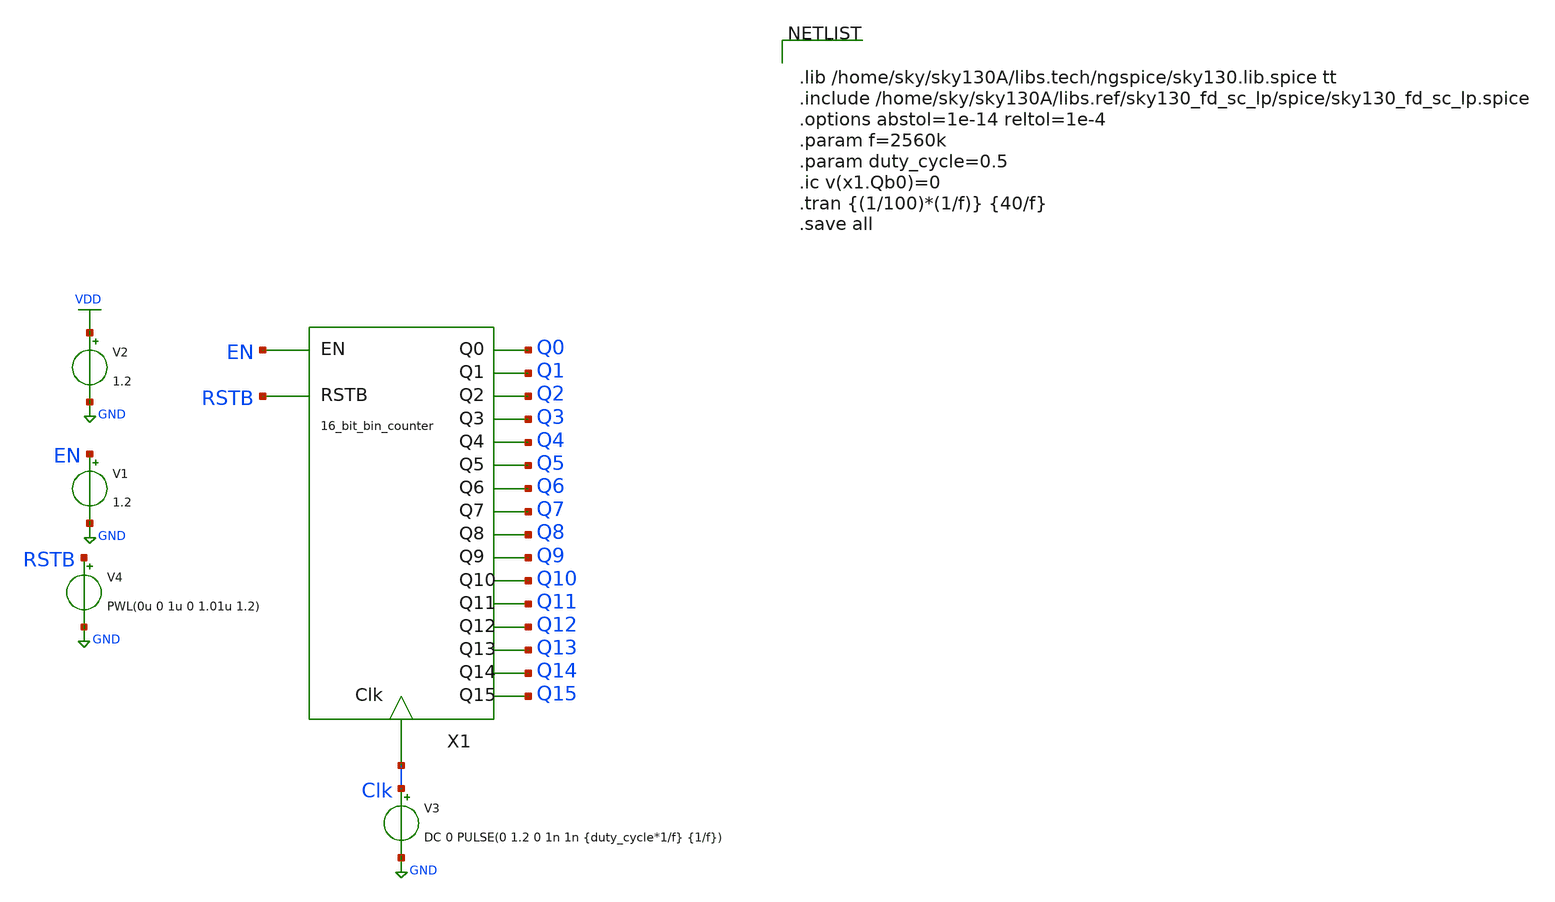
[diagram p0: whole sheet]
** sch_path: xschem/binary counter/bin_counter_tb.sch
**.subckt bin_counter_tb
V3 Clk GND DC 0 PULSE(0 1.2 0 1n 1n {duty_cycle*1/f} {1/f})
V1 EN GND 1.2
V2 VDD GND 1.2
X1 EN Q1 Q6 Clk Q0 Q2 Q3 Q4 Q5 Q7 Q8 Q9 Q10 Q11 Q12 Q13 Q14 Q15 RSTB bin_counter
V4 RSTB GND PWL(0u 0 1u 0 1.01u 1.2)
**** begin user architecture code


.lib /home/sky/sky130A/libs.tech/ngspice/sky130.lib.spice tt
.include /home/sky/sky130A/libs.ref/sky130_fd_sc_lp/spice/sky130_fd_sc_lp.spice
.options abstol=1e-14 reltol=1e-4
.param f=2560k
.param duty_cycle=0.5
.ic v(x1.Qb0)=0
.tran {(1/100)*(1/f)} {40/f}
.save all


**** end user architecture code
**.ends

* expanding   symbol:  binary counter/bin_counter.sym # of pins=19
** sym_path: xschem/binary counter/bin_counter.sym
** sch_path: xschem/binary counter/bin_counter.sch
.subckt bin_counter EN Q1 Q6 Clk Q0 Q2 Q3 Q4 Q5 Q7 Q8 Q9 Q10 Q11 Q12 Q13 Q14 Q15 RSTB
*.ipin Clk
*.ipin EN
*.opin Q0
*.opin Q1
*.opin Q2
*.opin Q4
*.opin Q5
*.opin Q6
*.opin Q7
*.opin Q3
*.opin Q8
*.opin Q9
*.opin Q10
*.opin Q12
*.opin Q13
*.opin Q14
*.opin Q11
*.opin Q15
*.ipin RSTB
x15 net1 Q1 GND GND VDD VDD net2 sky130_fd_sc_lp__and2_1
x7 net2 Q2 GND GND VDD VDD net3 sky130_fd_sc_lp__and2_1
x8 net4 Q4 GND GND VDD VDD net5 sky130_fd_sc_lp__and2_1
x9 net3 Q3 GND GND VDD VDD net4 sky130_fd_sc_lp__and2_1
x10 net5 Q5 GND GND VDD VDD net6 sky130_fd_sc_lp__and2_1
x11 net6 Q6 GND GND VDD VDD net7 sky130_fd_sc_lp__and2_1
x12 EN Q0 GND GND VDD VDD net1 sky130_fd_sc_lp__and2_1
x1 net8 Q9 GND GND VDD VDD net9 sky130_fd_sc_lp__and2_1
x2 net9 Q10 GND GND VDD VDD net10 sky130_fd_sc_lp__and2_1
x3 net11 Q12 GND GND VDD VDD net12 sky130_fd_sc_lp__and2_1
x4 net10 Q11 GND GND VDD VDD net11 sky130_fd_sc_lp__and2_1
x5 net12 Q13 GND GND VDD VDD net13 sky130_fd_sc_lp__and2_1
x6 net13 Q14 GND GND VDD VDD net14 sky130_fd_sc_lp__and2_1
x13 wire Q8 GND GND VDD VDD net8 sky130_fd_sc_lp__and2_1
x14 net7 Q7 GND GND VDD VDD wire sky130_fd_sc_lp__and2_1
X1 EN Q0 Clk RSTB asyn_rst_t_ff
X2 net1 Q1 Clk RSTB asyn_rst_t_ff
X3 net2 Q2 Clk RSTB asyn_rst_t_ff
X4 net3 Q3 Clk RSTB asyn_rst_t_ff
X5 net4 Q4 Clk RSTB asyn_rst_t_ff
X6 net5 Q5 Clk RSTB asyn_rst_t_ff
X7 net6 Q6 Clk RSTB asyn_rst_t_ff
X8 net7 Q7 Clk RSTB asyn_rst_t_ff
X9 wire Q8 Clk RSTB asyn_rst_t_ff
X10 net8 Q9 Clk RSTB asyn_rst_t_ff
X11 net9 Q10 Clk RSTB asyn_rst_t_ff
X12 net10 Q11 Clk RSTB asyn_rst_t_ff
X13 net11 Q12 Clk RSTB asyn_rst_t_ff
X14 net12 Q13 Clk RSTB asyn_rst_t_ff
X15 net13 Q14 Clk RSTB asyn_rst_t_ff
X16 net14 Q15 Clk RSTB asyn_rst_t_ff
.ends


* expanding   symbol:  T_flip_flop/asyn_rst_t_ff.sym # of pins=4
** sym_path: xschem/T_flip_flop/asyn_rst_t_ff.sym
** sch_path: xschem/T_flip_flop/asyn_rst_t_ff.sch
.subckt asyn_rst_t_ff T Q CLK RSTB
*.ipin T
*.ipin CLK
*.opin Q
*.ipin RSTB
x1 CLK net1 RSTB GND GND VDD VDD Q sky130_fd_sc_lp__dfrtp_1
x3 T Q GND GND VDD VDD net1 sky130_fd_sc_lp__xor2_1
.ends

.GLOBAL GND
.GLOBAL VDD
.end
